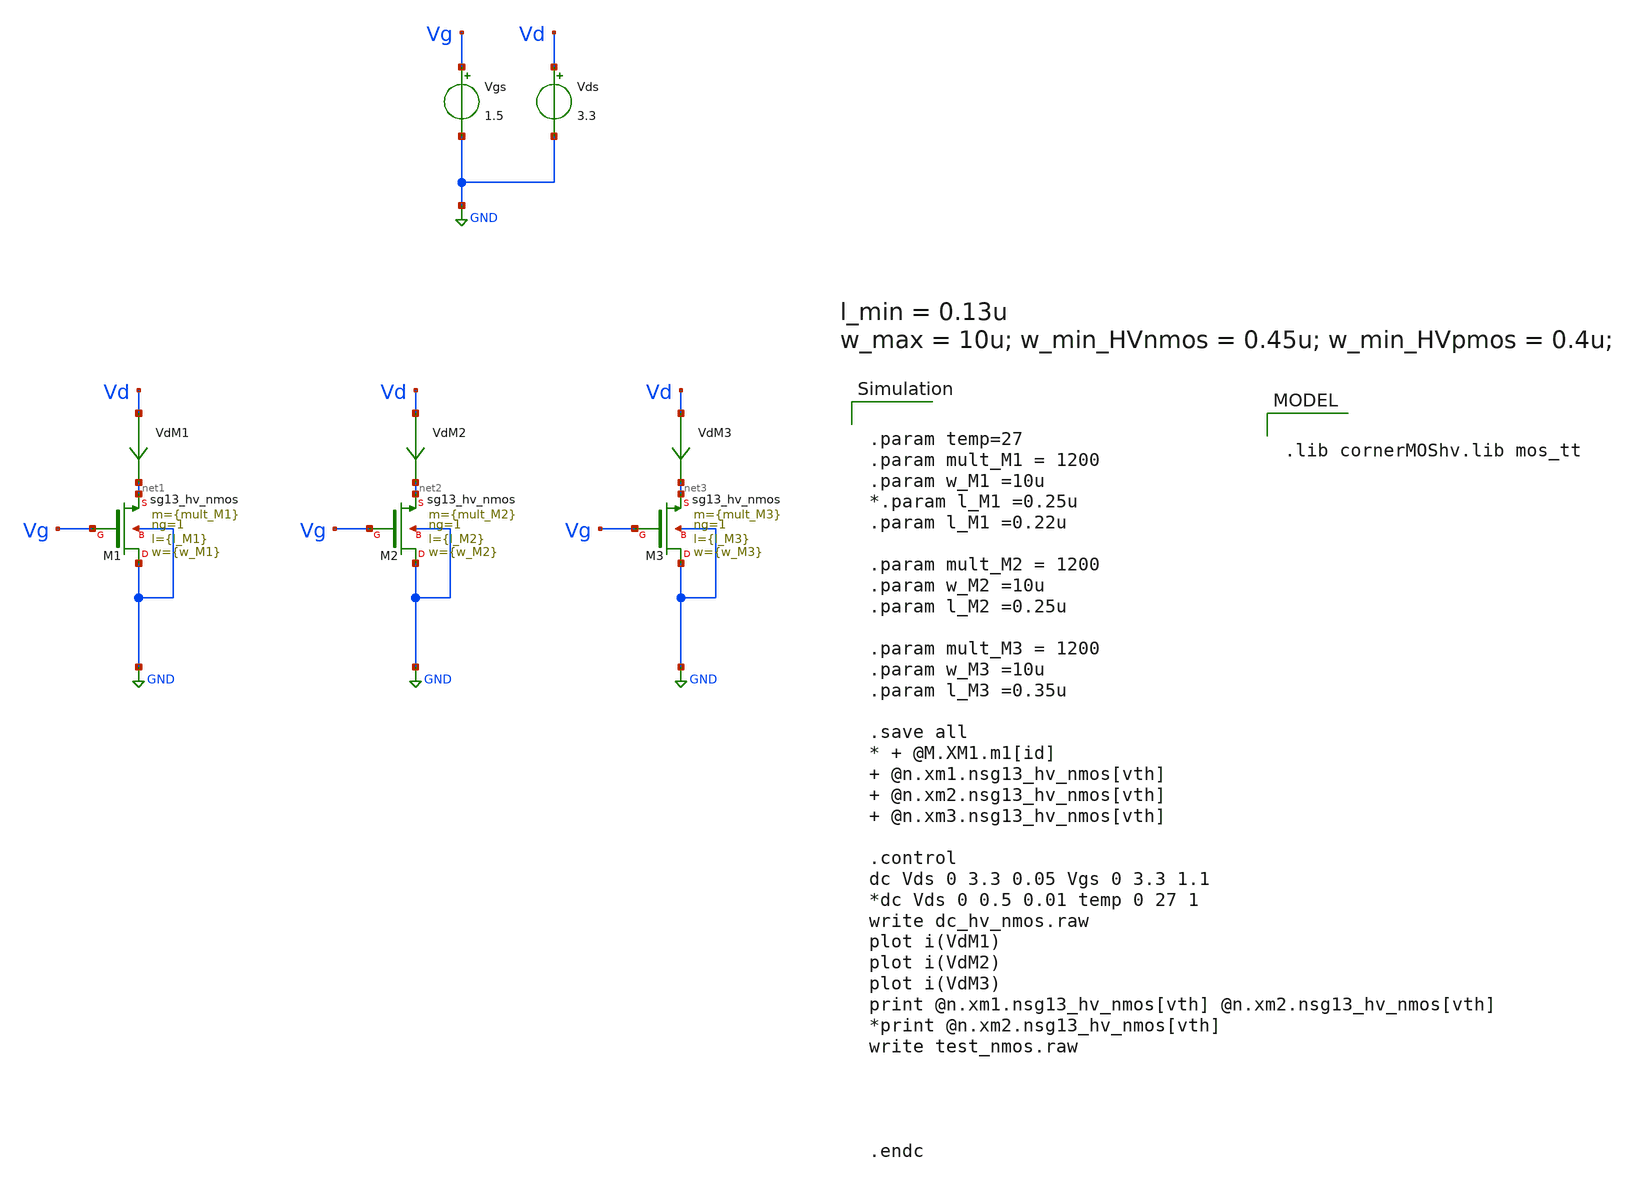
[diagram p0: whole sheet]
** sch_path: xschem/DCDCBuck/TB_hvNMOS_charact_v1p2.sch
**.subckt TB_hvNMOS_charact_v1p2
XM1 GND Vg net1 GND sg13_hv_nmos w={w_M1} l={l_M1} ng=1 m={mult_M1} mm_ok=1
Vgs Vg GND 1.5
Vds Vd GND 3.3
VdM1 Vd net1 0
.save i(vdm1)
XM2 GND Vg net2 GND sg13_hv_nmos w={w_M2} l={l_M2} ng=1 m={mult_M2} mm_ok=1
VdM2 Vd net2 0
.save i(vdm2)
XM3 GND Vg net3 GND sg13_hv_nmos w={w_M3} l={l_M3} ng=1 m={mult_M3} mm_ok=1
VdM3 Vd net3 0
.save i(vdm3)
**** begin user architecture code


.param temp=27
.param mult_M1 = 1200
.param w_M1 =10u
*.param l_M1 =0.25u
.param l_M1 =0.22u

.param mult_M2 = 1200
.param w_M2 =10u
.param l_M2 =0.25u

.param mult_M3 = 1200
.param w_M3 =10u
.param l_M3 =0.35u

.save all
* + @M.XM1.m1[id]  @n.xm1.nsg13_hv_nmos[vth]  @n.xm2.nsg13_hv_nmos[vth]  @n.xm3.nsg13_hv_nmos[vth]

.control
dc Vds 0 3.3 0.05 Vgs 0 3.3 1.1
*dc Vds 0 0.5 0.01 temp 0 27 1
write dc_hv_nmos.raw
plot i(VdM1)
plot i(VdM2)
plot i(VdM3)
print @n.xm1.nsg13_hv_nmos[vth] @n.xm2.nsg13_hv_nmos[vth]
*print @n.xm2.nsg13_hv_nmos[vth]
write test_nmos.raw




.endc



.lib cornerMOShv.lib mos_tt

**** end user architecture code
**.ends
.GLOBAL GND
.end
